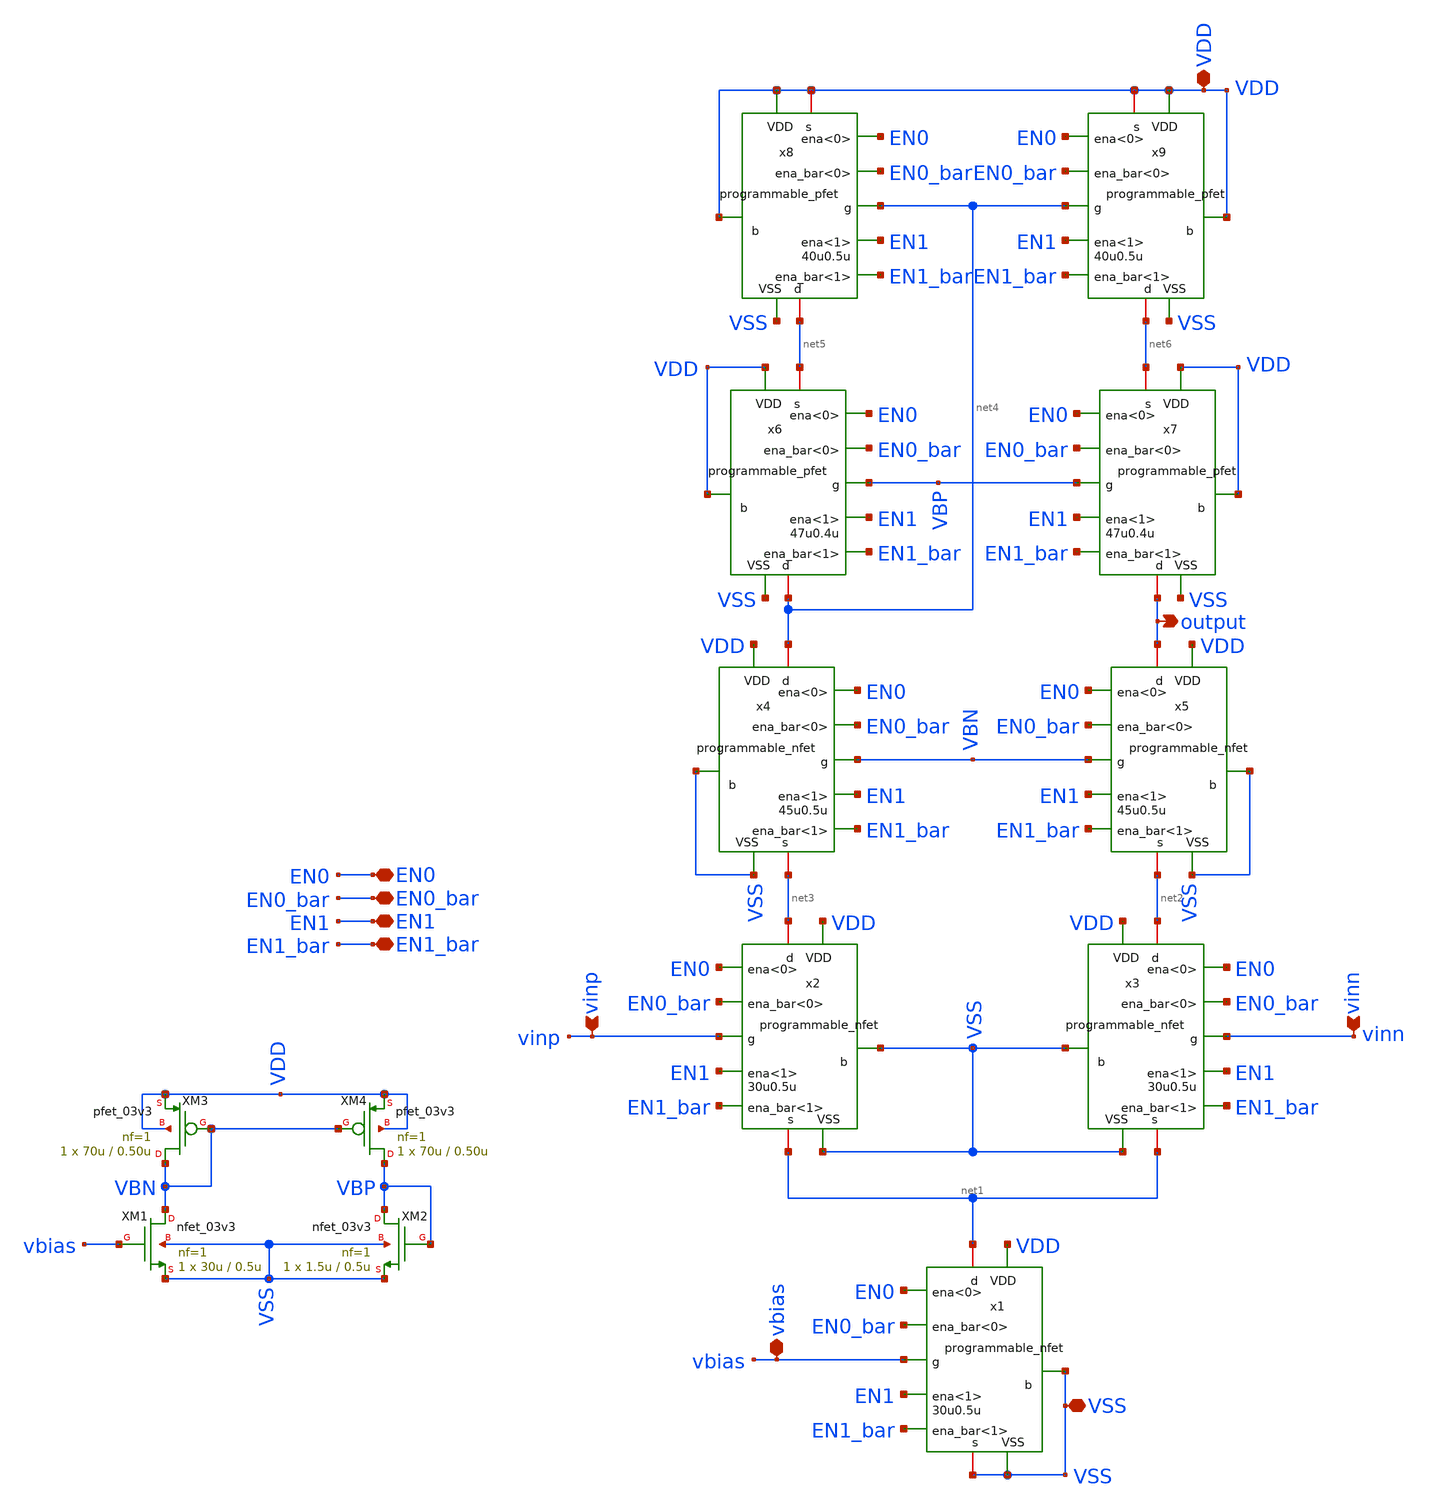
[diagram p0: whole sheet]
** sch_path: designs/libs/core_amps/ota_telescopic/programmable_telescopic_cascode.sch
**.subckt programmable_telescopic_cascode output VDD EN0_bar EN1 EN0 EN1_bar vinp vinn VSS vbias
*.opin output
*.iopin VDD
*.iopin EN0_bar
*.iopin EN1
*.iopin EN0
*.iopin EN1_bar
*.ipin vinp
*.ipin vinn
*.iopin VSS
*.iopin vbias
x1 net1 VSS vbias VSS EN0_bar VDD EN1_bar EN0 EN1 VSS programmable_nfet width=30u length=0.5u
x3 net2 VSS vinn net1 EN0_bar VDD EN1_bar EN0 EN1 VSS programmable_nfet width=30u length=0.5u
x2 net3 VSS vinp net1 EN0_bar VDD EN1_bar EN0 EN1 VSS programmable_nfet width=30u length=0.5u
x4 net4 VSS VBN net3 EN0_bar VDD EN1_bar EN0 EN1 VSS programmable_nfet width=45u length=0.5u
x5 output VSS VBN net2 EN0_bar VDD EN1_bar EN0 EN1 VSS programmable_nfet width=45u length=0.5u
x7 output VDD VBP net6 EN0_bar VDD EN1_bar EN0 EN1 VSS programmable_pfet width=47u length=0.4u
x6 net4 VDD VBP net5 EN0_bar VDD EN1_bar EN0 EN1 VSS programmable_pfet width=47u length=0.4u
x8 net5 VDD net4 VDD EN0_bar VDD EN1_bar EN0 EN1 VSS programmable_pfet width=40u length=0.5u
x9 net6 VDD net4 VDD EN0_bar VDD EN1_bar EN0 EN1 VSS programmable_pfet width=40u length=0.5u
XM1 VBN vbias VSS VSS nfet_03v3 L=0.5u W=30u nf=1 ad='int((nf+1)/2) * W/nf * 0.18u' as='int((nf+2)/2) * W/nf * 0.18u'
+ pd='2*int((nf+1)/2) * (W/nf + 0.18u)' ps='2*int((nf+2)/2) * (W/nf + 0.18u)' nrd='0.18u / W' nrs='0.18u / W'
+ sa=0 sb=0 sd=0 m=1
XM2 VBP VBP VSS VSS nfet_03v3 L=0.5u W=1.5u nf=1 ad='int((nf+1)/2) * W/nf * 0.18u' as='int((nf+2)/2) * W/nf * 0.18u'
+ pd='2*int((nf+1)/2) * (W/nf + 0.18u)' ps='2*int((nf+2)/2) * (W/nf + 0.18u)' nrd='0.18u / W' nrs='0.18u / W'
+ sa=0 sb=0 sd=0 m=1
XM4 VBP VBN VDD VDD pfet_03v3 L=0.50u W=70u nf=1 ad='int((nf+1)/2) * W/nf * 0.18u' as='int((nf+2)/2) * W/nf * 0.18u'
+ pd='2*int((nf+1)/2) * (W/nf + 0.18u)' ps='2*int((nf+2)/2) * (W/nf + 0.18u)' nrd='0.18u / W' nrs='0.18u / W'
+ sa=0 sb=0 sd=0 m=1
XM3 VBN VBN VDD VDD pfet_03v3 L=0.50u W=70u nf=1 ad='int((nf+1)/2) * W/nf * 0.18u' as='int((nf+2)/2) * W/nf * 0.18u'
+ pd='2*int((nf+1)/2) * (W/nf + 0.18u)' ps='2*int((nf+2)/2) * (W/nf + 0.18u)' nrd='0.18u / W' nrs='0.18u / W'
+ sa=0 sb=0 sd=0 m=1
**** begin user architecture code


.include /foss/pdks/gf180mcuD/libs.tech/ngspice/design.ngspice
.lib /foss/pdks/gf180mcuD/libs.tech/ngspice/sm141064.ngspice typical

**** end user architecture code
**.ends
.end
